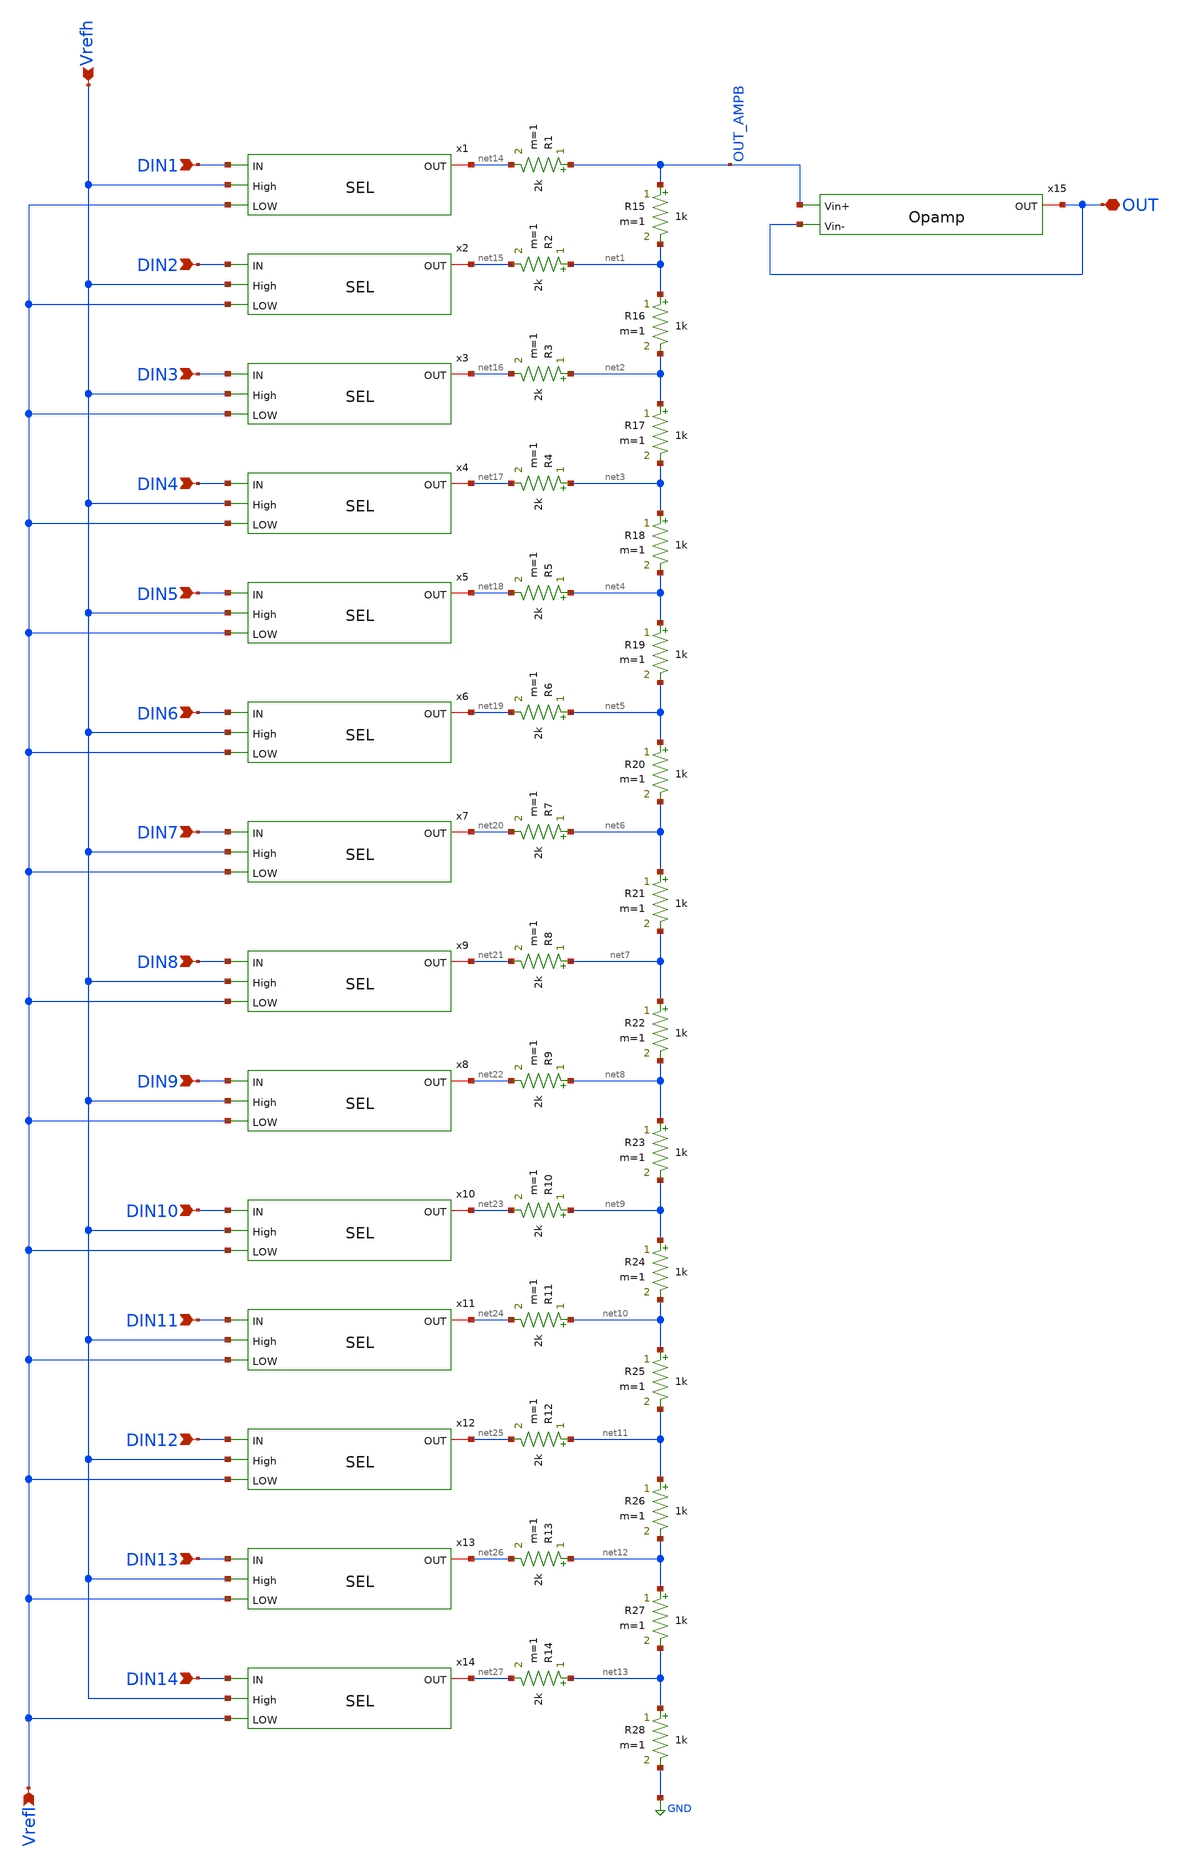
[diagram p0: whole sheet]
** sch_path: LR_Work2/RDAC.sch
**.subckt RDAC Vrefh Vrefl OUT DIN1 DIN2 DIN3 DIN4 DIN5 DIN6 DIN7 DIN8 DIN9 DIN10 DIN11 DIN12 DIN13
*+ DIN14
*.ipin Vrefh
*.ipin Vrefl
*.iopin OUT
*.ipin DIN1
*.ipin DIN2
*.ipin DIN3
*.ipin DIN4
*.ipin DIN5
*.ipin DIN6
*.ipin DIN7
*.ipin DIN8
*.ipin DIN9
*.ipin DIN10
*.ipin DIN11
*.ipin DIN12
*.ipin DIN13
*.ipin DIN14
R1 OUT_AMPB net14 2k m=1
R2 net1 net15 2k m=1
R3 net2 net16 2k m=1
R4 net3 net17 2k m=1
R5 net4 net18 2k m=1
R6 net5 net19 2k m=1
R7 net6 net20 2k m=1
R8 net7 net21 2k m=1
R9 net8 net22 2k m=1
R10 net9 net23 2k m=1
R11 net10 net24 2k m=1
R12 net11 net25 2k m=1
R13 net12 net26 2k m=1
R14 net13 net27 2k m=1
R15 OUT_AMPB net1 1k m=1
R16 net1 net2 1k m=1
R17 net2 net3 1k m=1
R18 net3 net4 1k m=1
R19 net4 net5 1k m=1
R20 net5 net6 1k m=1
R21 net6 net7 1k m=1
R22 net7 net8 1k m=1
R23 net8 net9 1k m=1
R24 net9 net10 1k m=1
R25 net10 net11 1k m=1
R26 net11 net12 1k m=1
R27 net12 net13 1k m=1
R28 net13 GND 1k m=1
x1 DIN1 Vrefh net14 Vrefl SEL
x2 DIN2 Vrefh net15 Vrefl SEL
x3 DIN3 Vrefh net16 Vrefl SEL
x4 DIN4 Vrefh net17 Vrefl SEL
x5 DIN5 Vrefh net18 Vrefl SEL
x6 DIN6 Vrefh net19 Vrefl SEL
x7 DIN7 Vrefh net20 Vrefl SEL
x8 DIN9 Vrefh net22 Vrefl SEL
x9 DIN8 Vrefh net21 Vrefl SEL
x10 DIN10 Vrefh net23 Vrefl SEL
x11 DIN11 Vrefh net24 Vrefl SEL
x12 DIN12 Vrefh net25 Vrefl SEL
x13 DIN13 Vrefh net26 Vrefl SEL
x14 DIN14 Vrefh net27 Vrefl SEL
x15 OUT_AMPB OUT OUT Opamp
**** begin user architecture code


VVDD VDD 0 dc 3.3
VVrefh Vrefh 0 dc 3.3
VVrefl Vrefl 0 dc 0

VDIN1 DIN1 0 pulse(0 3.3 100n 1n 1n 100n 400n)
VDIN2 DIN2 0 pulse(0 3.3 100n 1n 1n 200n 300n)
VDIN3 DIN3 0 pulse(0 3.3 100n 1n 1n 300n 500n)
VDIN4 DIN4 0 pulse(0 3.3 100n 1n 1n 300n 500n)
VDIN5 DIN5 0 pulse(0 3.3 100n 1n 1n 300n 500n)
VDIN6 DIN6 0 pulse(0 3.3 100n 1n 1n 400n 500n)
VDIN7 DIN7 0 pulse(0 3.3 100n 1n 1n 300n 500n)
VDIN8 DIN8 0 pulse(0 3.3 100n 1n 1n 300n 500n)
VDIN9 DIN9 0 pulse(0 3.3 100n 1n 1n 300n 500n)
VDIN10 DIN10 0 pulse(0 3.3 100n 1n 1n 400n 500n)
VDIN11 DIN11 0 pulse(0 3.3 100n 1n 1n 300n 500n)
VDIN12 DIN12 0 pulse(0 3.3 100n 1n 1n 300n 500n)
VDIN13 DIN13 0 pulse(0 3.3 100n 1n 1n 300n 500n)
VDIN14 DIN14 0 pulse(0 3.3 100n 1n 1n 400n 500n)

.MODEL nmos NMOS (     LEVEL   = 49 VERSION = 3.1            TNOM    = 27             TOX     =
+ 7.6E-9 XJ      = 1.5E-7         NCH     = 1.7E17         VTH0    = 0.4964448 K1      = 0.5307769      K2
+      = 0.0199705      K3      = 0.2963637 K3B     = 0.2012165      W0      = 2.836319E-6    NLX     =
+ 2.894802E-7 DVT0W   = 0              DVT1W   = 5.3E6          DVT2W   = -0.032 DVT0    = 0.112017       DVT1
+    = 0.2453972      DVT2    = -0.171915 U0      = 444.9381976    UA      = 2.921284E-10   UB      =
+ 1.773281E-18 UC      = 7.067896E-11   VSAT    = 1.130785E5     A0      = 1.1356246 AGS     = 0.2810374      B0
+      = 2.844393E-7    B1      = 5E-6 KETA    = -7.8181E-3     A1      = 0              A2      = 1 RDSW
+    = 925.2701982    PRWG    = -1E-3          PRWB    = -1E-3 WR      = 1              WINT    =
+ 7.186965E-8    LINT    = 1.735515E-9 XL      = -2E-8          XW      = 0              DWG     = -1.712973E-8
+ DWB     = 5.851691E-9    VOFF    = -0.132935      NFACTOR = 0.5710974 CIT     = 0              CDSC
+    = 8.607229E-4    CDSCD   = 0 CDSCB   = 0              ETA0    = 2.128321E-3    ETAB    = 0 DSUB    =
+ 0.0257957      PCLM    = 0.6766314      PDIBLC1 = 1 PDIBLC2 = 1.787424E-3    PDIBLCB = 0              DROUT
+   = 0.7873539 PSCBE1  = 6.973485E9     PSCBE2  = 1.46235E-7     PVAG    = 0.05 DELTA   = 0.01
+           MOBMOD  = 1              PRT     = 0 UTE     = -1.5           KT1     = -0.11          KT1L    = 0 KT2
+     = 0.022          UA1     = 4.31E-9        UB1     = -7.61E-18 UC1     = -5.6E-11       AT      =
+ 3.3E4          WL      = 0 WLN     = 1              WW      = 0              WWN     = 1 WWL     = 0
+              LL      = 0              LLN     = 1 LW      = 0              LWN     = 1              LWL     = 0
+ CAPMOD  = 2              CGDO    = 1.96E-10       CGSO    = 1.96E-10 CGBO    = 0              CJ      =
+ 9.276962E-4    PB      = 0.8157962 MJ      = 0.3557696      CJSW    = 3.181055E-10   PBSW    = 0.6869149 MJSW
+    = 0.1            PVTH0   = -0.0252481     PRDSW   = -96.4502805 PK2     = -4.805372E-3   WKETA   =
+ -7.643187E-4   LKETA   = -0.0129496      )

.MODEL pmos PMOS (     LEVEL   = 49 VERSION = 3.1            TNOM    = 27             TOX     =
+ 7.6E-9 XJ      = 1.5E-7         NCH     = 1.7E17         VTH0    = -0.6636594 K1      = 0.4564781      K2
+      = -0.019447      K3      = 39.382919 K3B     = -2.8930965     W0      = 2.655585E-6    NLX     =
+ 1.51028E-7 DVT0W   = 0              DVT1W   = 5.3E6          DVT2W   = -0.032 DVT0    = 1.1744581      DVT1
+    = 0.7631128      DVT2    = -0.1035171 U0      = 151.3305606    UA      = 2.061211E-10   UB      =
+ 1.823477E-18 UC      = -8.97321E-12   VSAT    = 9.915604E4     A0      = 1.1210053 AGS     = 0.3961954      B0
+      = 6.493139E-7    B1      = 4.273215E-6 KETA    = -9.27E-3       A1      = 0              A2      = 1
+ RDSW    = 2.30725E3      PRWG    = -1E-3          PRWB    = 0 WR      = 1              WINT    =
+ 5.962233E-8    LINT    = 4.30928E-9 XL      = -2E-8          XW      = 0              DWG     = -1.596201E-8
+ DWB     = 1.378919E-8    VOFF    = -0.15          NFACTOR = 2 CIT     = 0              CDSC    =
+ 6.593084E-4    CDSCD   = 0 CDSCB   = 0              ETA0    = 0.0286461      ETAB    = 0 DSUB    = 0.2436027
+      PCLM    = 4.3597508      PDIBLC1 = 7.447024E-4 PDIBLC2 = 4.256073E-3    PDIBLCB = 0              DROUT
+   = 0.0120292 PSCBE1  = 1.347622E10    PSCBE2  = 5E-9           PVAG    = 3.669793 DELTA   = 0.01
+           MOBMOD  = 1              PRT     = 0 UTE     = -1.5           KT1     = -0.11          KT1L    = 0 KT2
+     = 0.022          UA1     = 4.31E-9        UB1     = -7.61E-18 UC1     = -5.6E-11       AT      =
+ 3.3E4          WL      = 0 WLN     = 1              WW      = 0              WWN     = 1 WWL     = 0
+              LL      = 0              LLN     = 1 LW      = 0              LWN     = 1              LWL     = 0
+ CAPMOD  = 2              CGDO    = 2.307E-10      CGSO    = 2.307E-10 CGBO    = 0              CJ      =
+ 1.420282E-3    PB      = 0.99 MJ      = 0.5490877      CJSW    = 4.773605E-10   PBSW    = 0.99 MJSW    =
+ 0.1997417      PVTH0   = 6.58707E-3     PRDSW   = -93.5582228 PK2     = 1.011593E-3    WKETA   = -0.0101398
+     LKETA   = 6.027967E-3     )

.control
save all
tran 1n 500n
plot V(OUT_AMPB)
*plot V(OUT)

write RDAC.raw

.endc

**** end user architecture code
**.ends
.GLOBAL GND
.end
